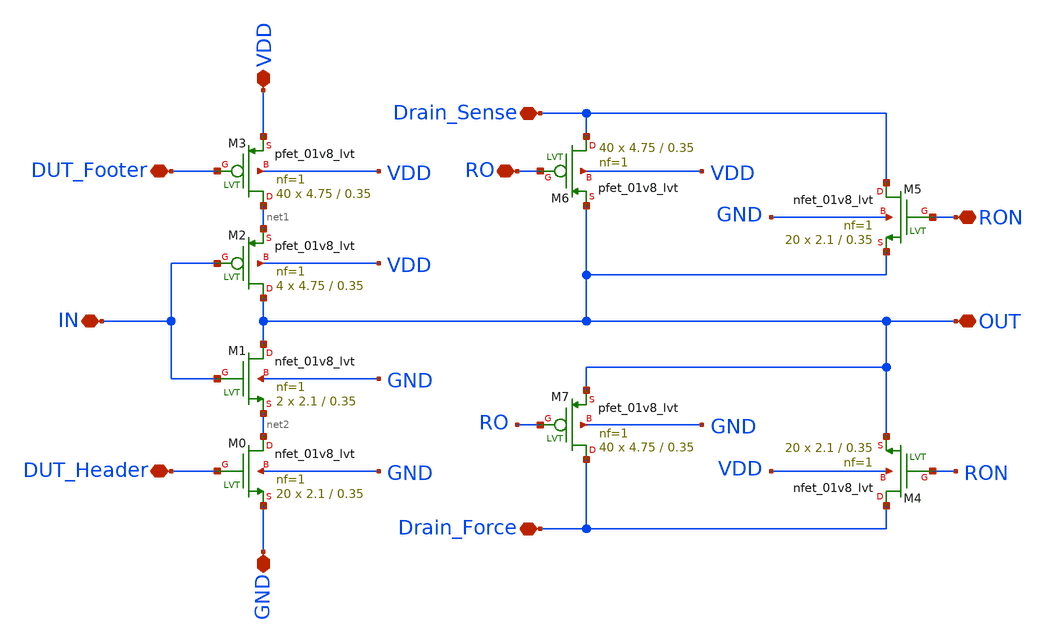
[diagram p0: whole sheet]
** sch_path: LVT/rovcel1_x10_LVT/rovcel1_x10_LVT.sch
**.subckt rovcel1_x10_LVT OUT Drain_Force DUT_Footer DUT_Header IN Drain_Sense VDD GND RO RON
*.iopin OUT
*.iopin Drain_Force
*.iopin DUT_Footer
*.iopin DUT_Header
*.iopin IN
*.iopin Drain_Sense
*.iopin VDD
*.iopin GND
*.iopin RO
*.iopin RON
XM0 net2 DUT_Header GND GND sky130_fd_pr__nfet_01v8_lvt L=0.35 W=2.1 nf=1 ad='int((nf+1)/2) * W/nf * 0.29'
+ as='int((nf+2)/2) * W/nf * 0.29' pd='2*int((nf+1)/2) * (W/nf + 0.29)' ps='2*int((nf+2)/2) * (W/nf + 0.29)'
+ nrd='0.29 / W' nrs='0.29 / W' sa=0 sb=0 sd=0 mult=20 m=20
XM1 OUT IN net2 GND sky130_fd_pr__nfet_01v8_lvt L=0.35 W=2.1 nf=1 ad='int((nf+1)/2) * W/nf * 0.29' as='int((nf+2)/2) * W/nf * 0.29'
+ pd='2*int((nf+1)/2) * (W/nf + 0.29)' ps='2*int((nf+2)/2) * (W/nf + 0.29)' nrd='0.29 / W' nrs='0.29 / W'
+ sa=0 sb=0 sd=0 mult=2 m=2
XM2 OUT IN net1 VDD sky130_fd_pr__pfet_01v8_lvt L=0.35 W=4.75 nf=1 ad='int((nf+1)/2) * W/nf * 0.29' as='int((nf+2)/2) * W/nf * 0.29'
+ pd='2*int((nf+1)/2) * (W/nf + 0.29)' ps='2*int((nf+2)/2) * (W/nf + 0.29)' nrd='0.29 / W' nrs='0.29 / W'
+ sa=0 sb=0 sd=0 mult=4 m=4
XM3 net1 DUT_Footer VDD VDD sky130_fd_pr__pfet_01v8_lvt L=0.35 W=4.75 nf=1 ad='int((nf+1)/2) * W/nf * 0.29'
+ as='int((nf+2)/2) * W/nf * 0.29' pd='2*int((nf+1)/2) * (W/nf + 0.29)' ps='2*int((nf+2)/2) * (W/nf + 0.29)'
+ nrd='0.29 / W' nrs='0.29 / W' sa=0 sb=0 sd=0 mult=40 m=40
XM4 Drain_Force RON OUT VDD sky130_fd_pr__nfet_01v8_lvt L=0.35 W=2.1 nf=1 ad='int((nf+1)/2) * W/nf * 0.29'
+ as='int((nf+2)/2) * W/nf * 0.29' pd='2*int((nf+1)/2) * (W/nf + 0.29)' ps='2*int((nf+2)/2) * (W/nf + 0.29)'
+ nrd='0.29 / W' nrs='0.29 / W' sa=0 sb=0 sd=0 mult=20 m=20
XM5 Drain_Sense RON OUT GND sky130_fd_pr__nfet_01v8_lvt L=0.35 W=2.1 nf=1 ad='int((nf+1)/2) * W/nf * 0.29'
+ as='int((nf+2)/2) * W/nf * 0.29' pd='2*int((nf+1)/2) * (W/nf + 0.29)' ps='2*int((nf+2)/2) * (W/nf + 0.29)'
+ nrd='0.29 / W' nrs='0.29 / W' sa=0 sb=0 sd=0 mult=20 m=20
XM6 Drain_Sense RO OUT VDD sky130_fd_pr__pfet_01v8_lvt L=0.35 W=4.75 nf=1 ad='int((nf+1)/2) * W/nf * 0.29'
+ as='int((nf+2)/2) * W/nf * 0.29' pd='2*int((nf+1)/2) * (W/nf + 0.29)' ps='2*int((nf+2)/2) * (W/nf + 0.29)'
+ nrd='0.29 / W' nrs='0.29 / W' sa=0 sb=0 sd=0 mult=40 m=40
XM7 Drain_Force RO OUT GND sky130_fd_pr__pfet_01v8_lvt L=0.35 W=4.75 nf=1 ad='int((nf+1)/2) * W/nf * 0.29'
+ as='int((nf+2)/2) * W/nf * 0.29' pd='2*int((nf+1)/2) * (W/nf + 0.29)' ps='2*int((nf+2)/2) * (W/nf + 0.29)'
+ nrd='0.29 / W' nrs='0.29 / W' sa=0 sb=0 sd=0 mult=40 m=40
**.ends
.end
